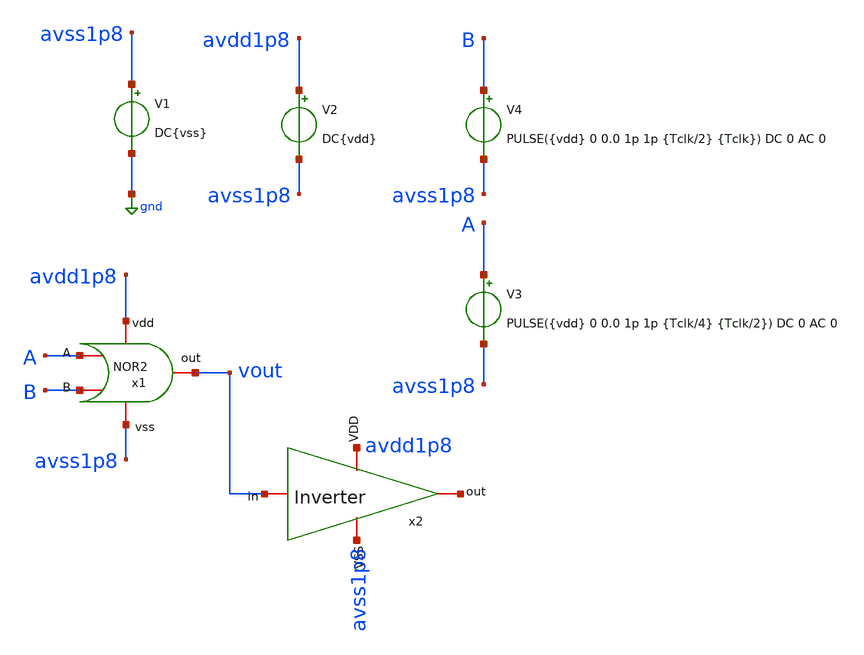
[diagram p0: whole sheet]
** sch_path: verification/testbenches/tb_nor2.sch
**.subckt tb_nor2
V1 avss1p8 gnd DC{vss}
V2 avdd1p8 avss1p8 DC{vdd}
V3 A avss1p8 PULSE({vdd} 0 0.0 1p 1p {Tclk/4} {Tclk/2}) DC 0 AC 0
V4 B avss1p8 PULSE({vdd} 0 0.0 1p 1p {Tclk/2} {Tclk}) DC 0 AC 0
x1 avdd1p8 B A vout avss1p8 nor2
x2 avdd1p8 net1 vout avss1p8 inverter
**** begin user architecture code


* Circuit Parameters
.param vdd = 1.2
.param vss = 0.0
.param Tclk = 10n
.options TEMP = 27.0
* Include Models - IHP SG13G2
.lib cornerMOSlv.lib mos_tt
* OP Parameters & Singals to save
.save all
*Simulations
.control
tran 0.01u 20n
setplot tran1
plot v(A) v(B)+1.5 v(vout)+3
reset
set filetype = ascii
write dcsweep.raw
.endc
.end


**** end user architecture code
**.ends

* expanding   symbol:  blocks/nor2/schematic/nor2.sym # of pins=5
** sym_path: design/blocks/nor2/schematic/nor2.sym
** sch_path: design/blocks/nor2/schematic/nor2.sch
.subckt nor2 vdd A B out vss
*.iopin vdd
*.iopin A
*.iopin B
*.iopin vss
*.iopin out
XM1 out B vss vss sg13_lv_nmos w=0.75u l=0.15u ng=1 m=1 mm_ok=1
XM2 out A vss vss sg13_lv_nmos w=0.75u l=0.15u ng=1 m=1 mm_ok=1
XM3 out B net1 vdd sg13_lv_pmos w=3u l=0.15u ng=1 m=1 mm_ok=1
XM4 net1 A vdd vdd sg13_lv_pmos w=3u l=0.15u ng=1 m=1 mm_ok=1
.ends


* expanding   symbol:  blocks/inverter/schematic/inverter.sym # of pins=4
** sym_path: design/blocks/inverter/schematic/inverter.sym
** sch_path: design/blocks/inverter/schematic/inverter.sch
.subckt inverter VDD out in VSS
*.iopin VDD
*.iopin in
*.iopin out
*.iopin VSS
XM3 out in VDD VDD sg13_lv_pmos w=1.5u l=0.15u ng=1 m=1 mm_ok=1
XM4 out in VSS VSS sg13_lv_nmos w=0.75u l=0.15u ng=1 m=1 mm_ok=1
.ends

.GLOBAL gnd
.end
